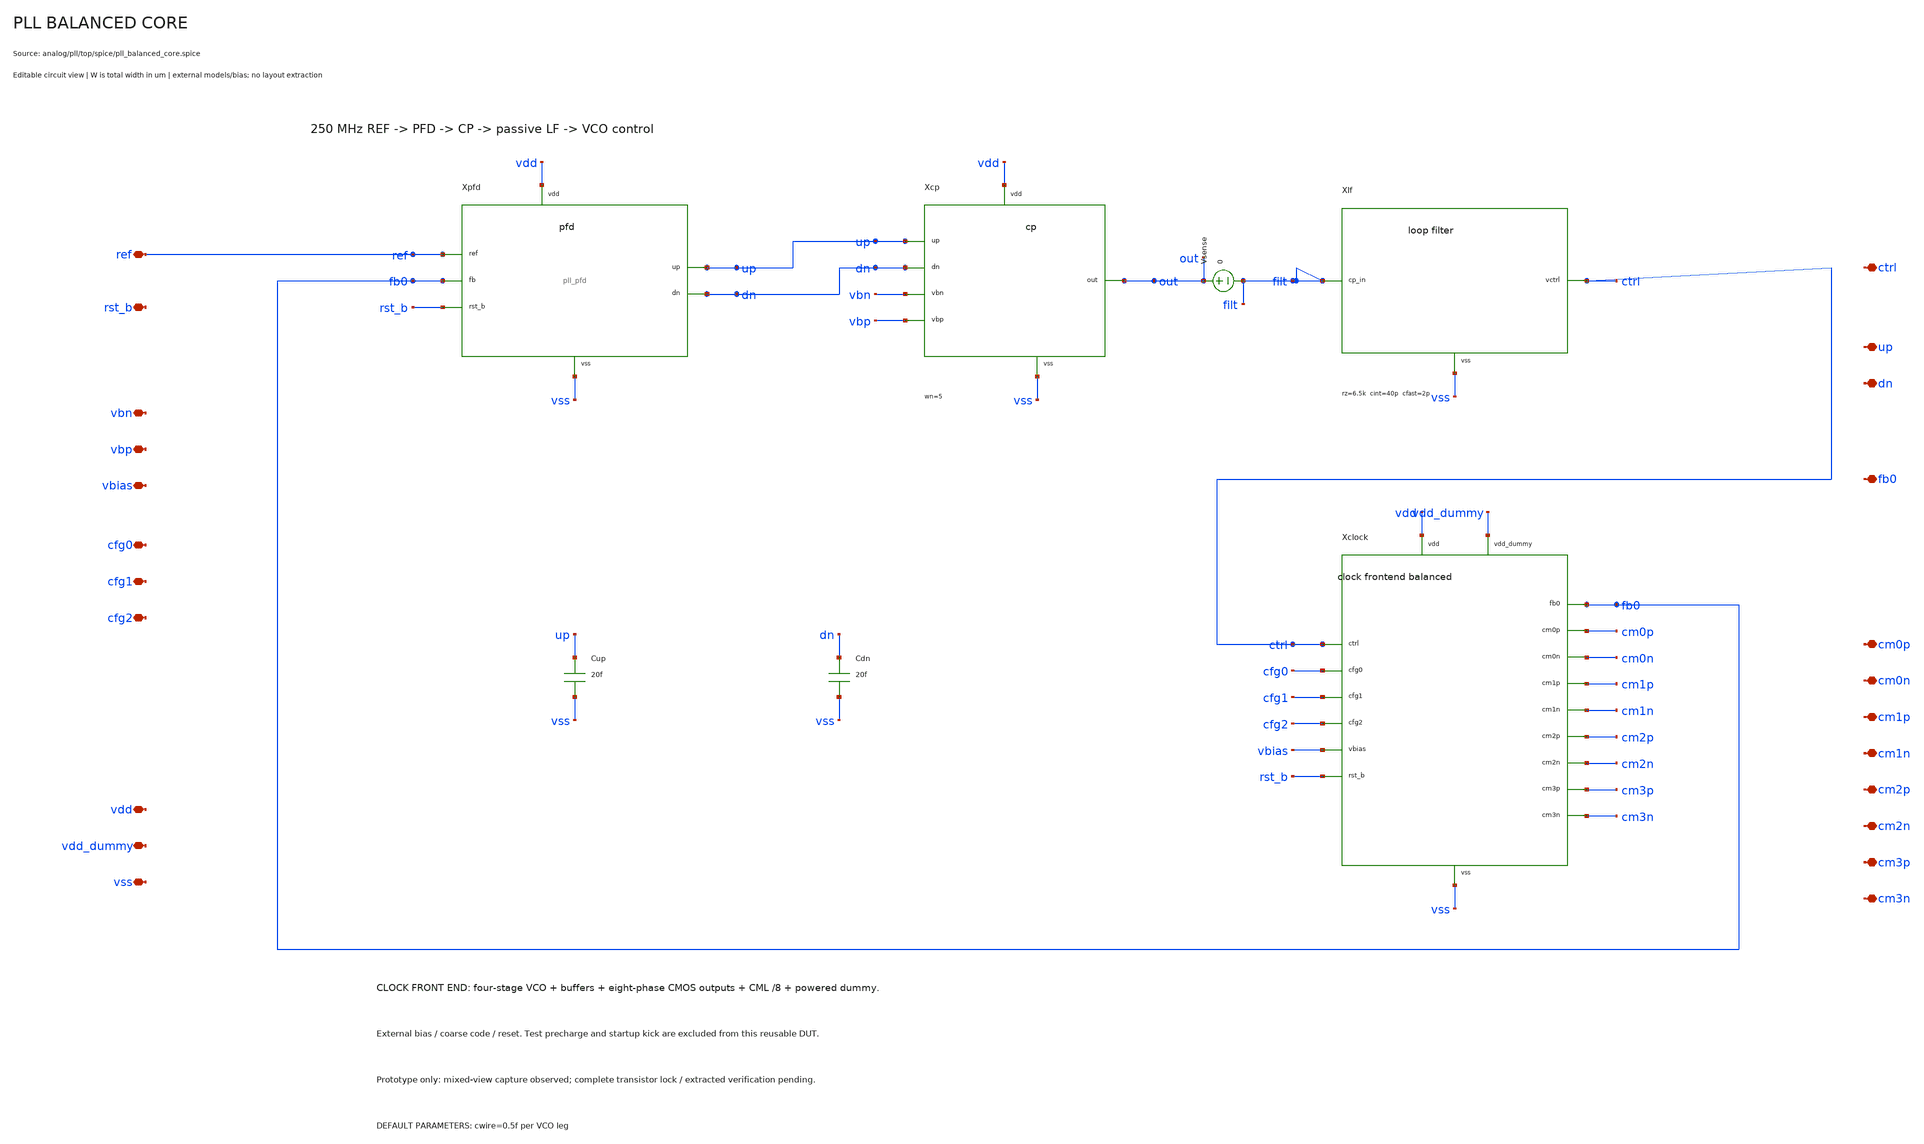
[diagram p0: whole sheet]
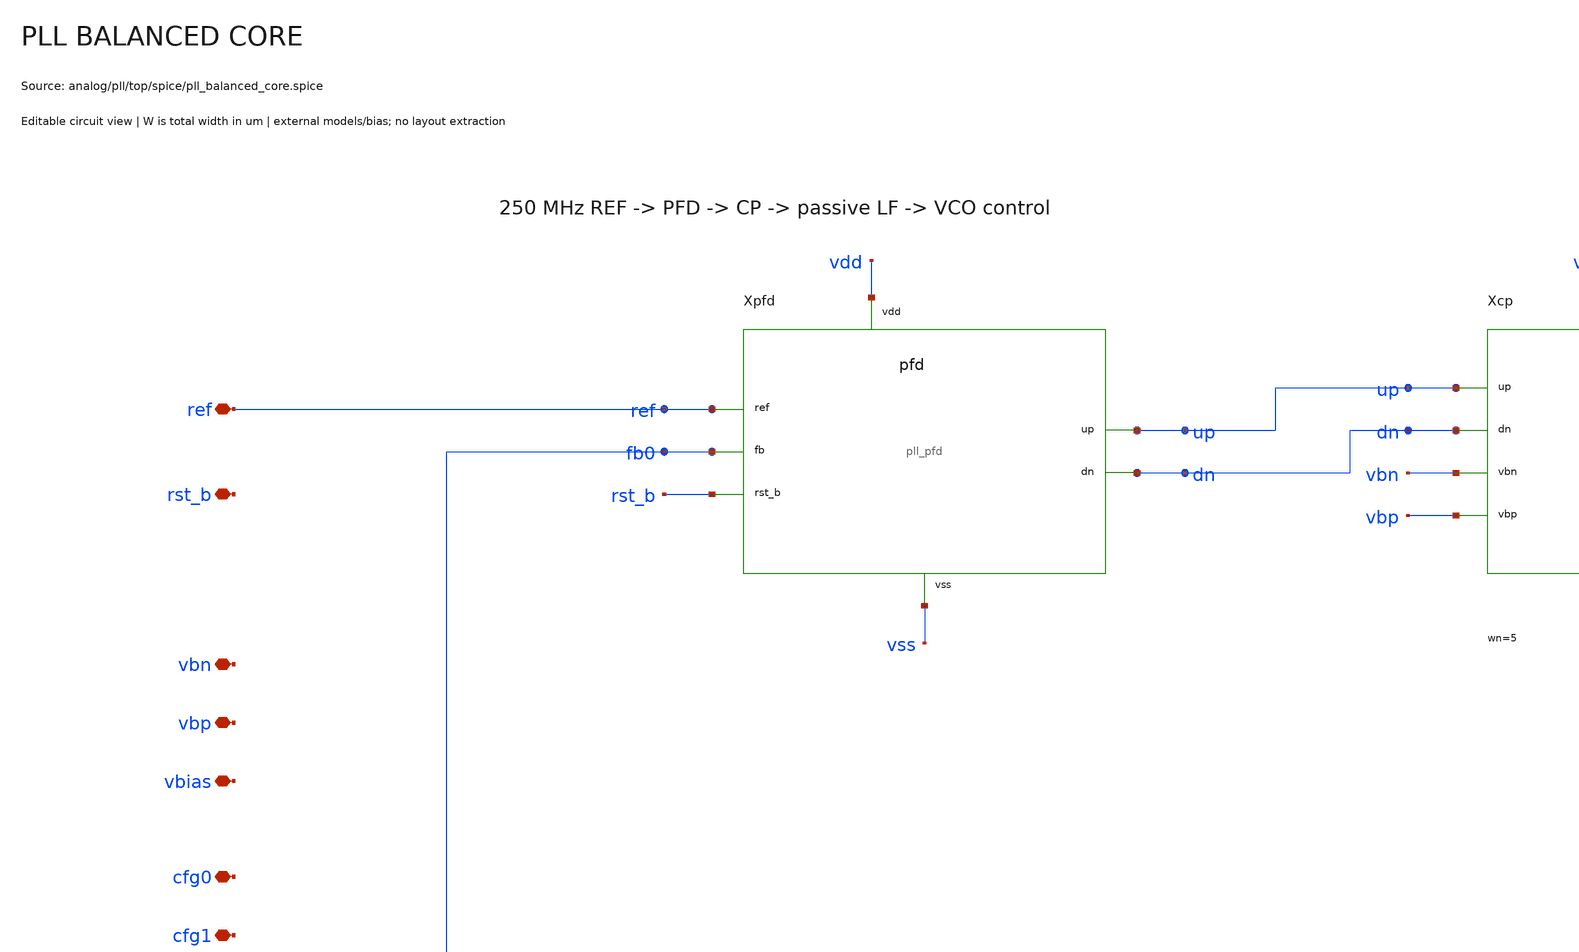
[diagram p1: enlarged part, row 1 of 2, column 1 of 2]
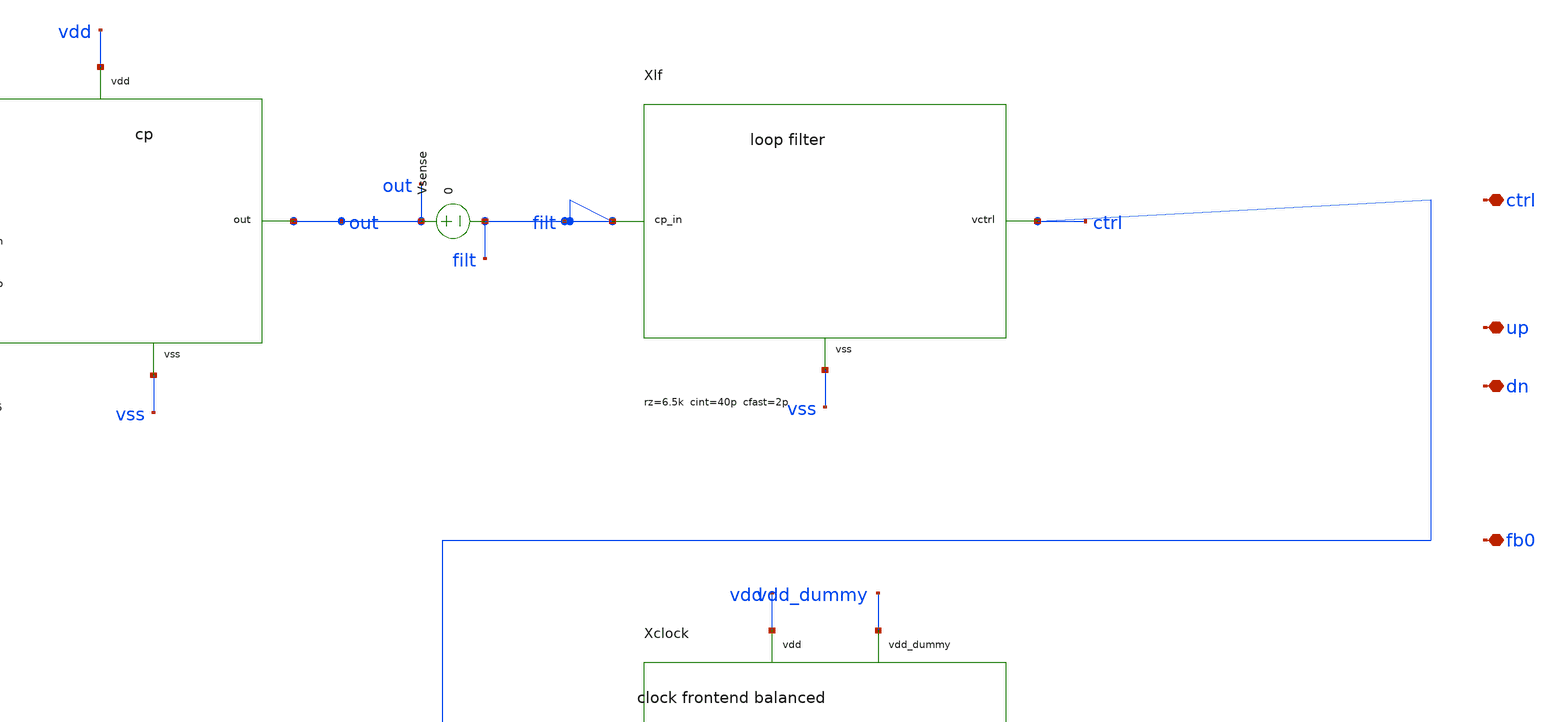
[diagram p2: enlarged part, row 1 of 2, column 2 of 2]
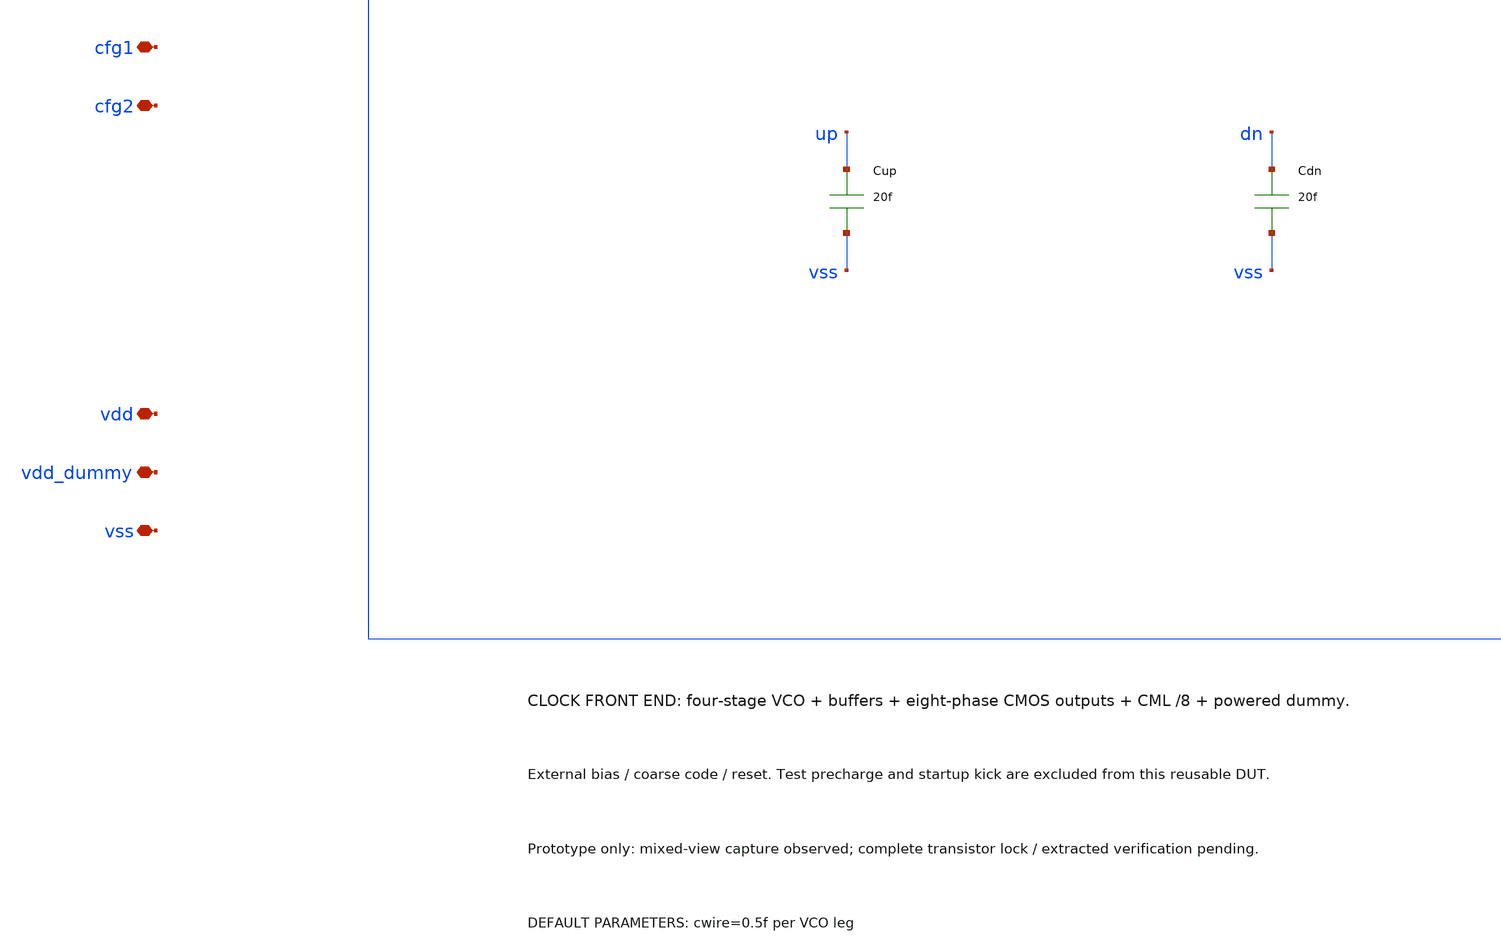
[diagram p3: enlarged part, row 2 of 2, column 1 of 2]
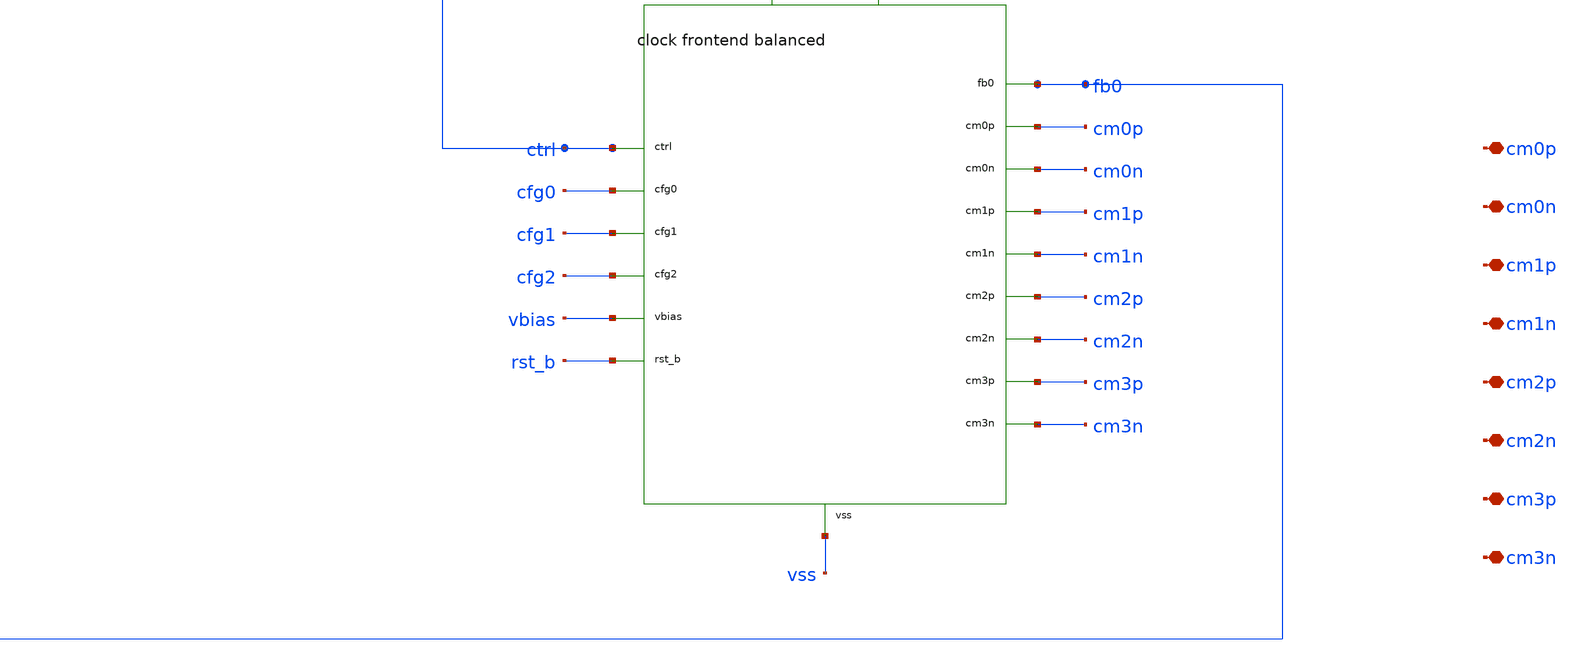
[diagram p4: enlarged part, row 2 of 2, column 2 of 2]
** sch_path: analog/pll/top/schematic/pll_balanced_core.sch
**.subckt pll_balanced_core ref rst_b vbn vbp vbias cfg0 cfg1 cfg2 ctrl up dn fb0 cm0p cm0n cm1p
*+ cm1n cm2p cm2n cm3p cm3n vdd vdd_dummy vss
*.iopin ref
*.iopin rst_b
*.iopin vbn
*.iopin vbp
*.iopin vbias
*.iopin cfg0
*.iopin cfg1
*.iopin cfg2
*.iopin ctrl
*.iopin up
*.iopin dn
*.iopin fb0
*.iopin cm0p
*.iopin cm0n
*.iopin cm1p
*.iopin cm1n
*.iopin cm2p
*.iopin cm2n
*.iopin cm3p
*.iopin cm3n
*.iopin vdd
*.iopin vdd_dummy
*.iopin vss
Xpfd ref fb0 rst_b up dn vdd vss pll_pfd reset_cap=5f out_wn=4 out_wp=8
Xcp up dn out vbn vbp vdd vss pll_cp wn=5 wp=20 lmirror=1 wsn=2 wsp=4 up_wn=0.5 up_wp=2 up_ln=0.88
Vsense out filt 0
Xlf filt ctrl vss pll_loop_filter rz=6.5k cint=40p cfast=2p
Xclock ctrl cfg0 cfg1 cfg2 vbias rst_b fb0 cm0p cm0n cm1p cm1n cm2p cm2n cm3p cm3n vdd vdd_dummy vss
+ pll_clock_frontend_balanced cwire={cwire}
Cup up vss 20f
Cdn dn vss 20f
**.ends
.end
